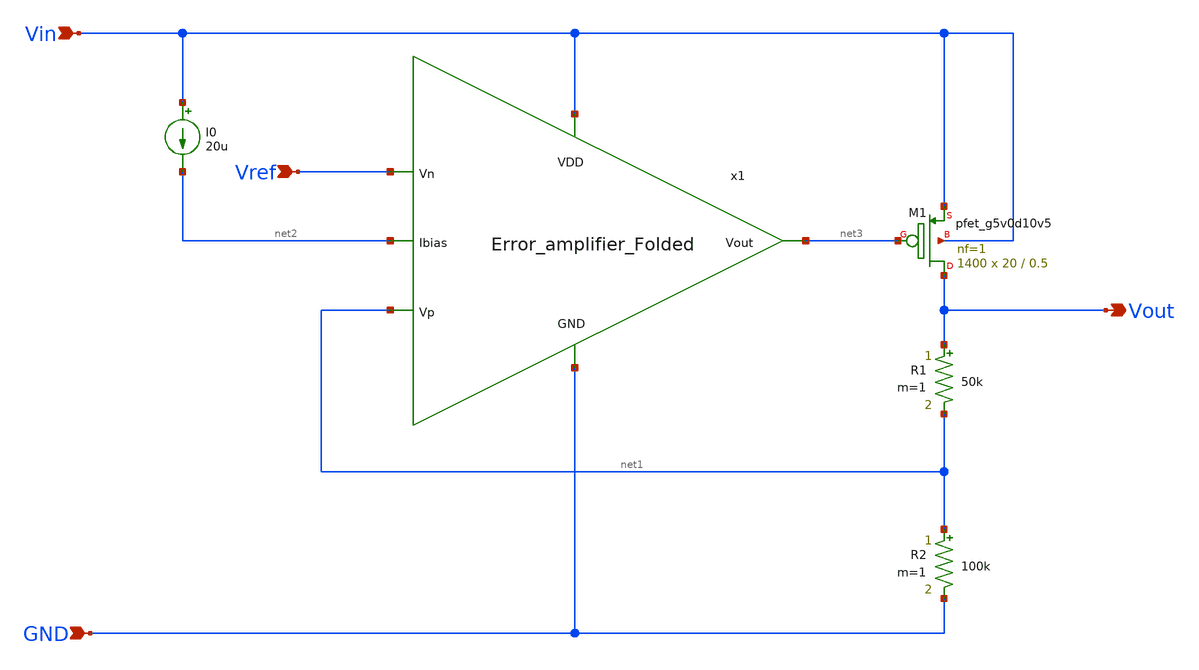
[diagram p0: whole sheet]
** sch_path: Analog_Blocks/LDO/Schematic/LDO_Miller_1.8v/LDO_test.sch
**.subckt LDO_test Vin GND Vout Vref
*.ipin Vin
*.ipin GND
*.opin Vout
*.ipin Vref
XM1 Vout net3 Vin Vin sky130_fd_pr__pfet_g5v0d10v5 L=0.5 W=20 nf=1 ad='int((nf+1)/2) * W/nf * 0.29' as='int((nf+2)/2) * W/nf * 0.29'
+ pd='2*int((nf+1)/2) * (W/nf + 0.29)' ps='2*int((nf+2)/2) * (W/nf + 0.29)' nrd='0.29 / W' nrs='0.29 / W'
+ sa=0 sb=0 sd=0 mult=1400 m=1400
R1 Vout net1 50k m=1
R2 net1 GND 100k m=1
I0 Vin net2 20u
x1 Vin net3 net1 Vref net2 GND Error_amplifier_Folded
**.ends

* expanding   symbol:
*+  /home/eslam/mabrains/Analog_blocks/Analog_Blocks/LDO/Schematic/LDO_Folded_1.8v/Error_amplifier_Folded.sym # of pins=6
** sym_path: Analog_Blocks/LDO/Schematic/LDO_Folded_1.8v/Error_amplifier_Folded.sym
** sch_path: Analog_Blocks/LDO/Schematic/LDO_Folded_1.8v/Error_amplifier_Folded.sch
.subckt Error_amplifier_Folded VDD Vout Vp Vn Ibias GND
*.ipin VDD
*.ipin GND
*.ipin Vp
*.ipin Vn
*.opin Vout
*.ipin Ibias
XM1 net3 Vp net1 GND sky130_fd_pr__nfet_g5v0d10v5 L=0.5 W=50 nf=1 ad='int((nf+1)/2) * W/nf * 0.29' as='int((nf+2)/2) * W/nf * 0.29'
+ pd='2*int((nf+1)/2) * (W/nf + 0.29)' ps='2*int((nf+2)/2) * (W/nf + 0.29)' nrd='0.29 / W' nrs='0.29 / W'
+ sa=0 sb=0 sd=0 mult=1 m=1
XM2 net2 Vn net1 GND sky130_fd_pr__nfet_g5v0d10v5 L=0.5 W=50 nf=1 ad='int((nf+1)/2) * W/nf * 0.29' as='int((nf+2)/2) * W/nf * 0.29'
+ pd='2*int((nf+1)/2) * (W/nf + 0.29)' ps='2*int((nf+2)/2) * (W/nf + 0.29)' nrd='0.29 / W' nrs='0.29 / W'
+ sa=0 sb=0 sd=0 mult=1 m=1
XM9 Vout net4 GND GND sky130_fd_pr__nfet_g5v0d10v5 L=2 W=6 nf=1 ad='int((nf+1)/2) * W/nf * 0.29' as='int((nf+2)/2) * W/nf * 0.29'
+ pd='2*int((nf+1)/2) * (W/nf + 0.29)' ps='2*int((nf+2)/2) * (W/nf + 0.29)' nrd='0.29 / W' nrs='0.29 / W'
+ sa=0 sb=0 sd=0 mult=1 m=1
XM6 net4 net6 net3 VDD sky130_fd_pr__pfet_g5v0d10v5 L=0.5 W=40 nf=1 ad='int((nf+1)/2) * W/nf * 0.29'
+ as='int((nf+2)/2) * W/nf * 0.29' pd='2*int((nf+1)/2) * (W/nf + 0.29)' ps='2*int((nf+2)/2) * (W/nf + 0.29)'
+ nrd='0.29 / W' nrs='0.29 / W' sa=0 sb=0 sd=0 mult=1 m=1
XM5 net2 net5 VDD VDD sky130_fd_pr__pfet_g5v0d10v5 L=0.5 W=40 nf=1 ad='int((nf+1)/2) * W/nf * 0.29' as='int((nf+2)/2) * W/nf * 0.29'
+ pd='2*int((nf+1)/2) * (W/nf + 0.29)' ps='2*int((nf+2)/2) * (W/nf + 0.29)' nrd='0.29 / W' nrs='0.29 / W'
+ sa=0 sb=0 sd=0 mult=1 m=1
XM4 net3 net5 VDD VDD sky130_fd_pr__pfet_g5v0d10v5 L=0.5 W=40 nf=1 ad='int((nf+1)/2) * W/nf * 0.29' as='int((nf+2)/2) * W/nf * 0.29'
+ pd='2*int((nf+1)/2) * (W/nf + 0.29)' ps='2*int((nf+2)/2) * (W/nf + 0.29)' nrd='0.29 / W' nrs='0.29 / W'
+ sa=0 sb=0 sd=0 mult=1 m=1
XM3 net1 Ibias GND GND sky130_fd_pr__nfet_g5v0d10v5 L=0.9 W=12 nf=1 ad='int((nf+1)/2) * W/nf * 0.29'
+ as='int((nf+2)/2) * W/nf * 0.29' pd='2*int((nf+1)/2) * (W/nf + 0.29)' ps='2*int((nf+2)/2) * (W/nf + 0.29)'
+ nrd='0.29 / W' nrs='0.29 / W' sa=0 sb=0 sd=0 mult=1 m=1
XM7 Vout net6 net2 VDD sky130_fd_pr__pfet_g5v0d10v5 L=0.5 W=40 nf=1 ad='int((nf+1)/2) * W/nf * 0.29'
+ as='int((nf+2)/2) * W/nf * 0.29' pd='2*int((nf+1)/2) * (W/nf + 0.29)' ps='2*int((nf+2)/2) * (W/nf + 0.29)'
+ nrd='0.29 / W' nrs='0.29 / W' sa=0 sb=0 sd=0 mult=1 m=1
XM8 net4 net4 GND GND sky130_fd_pr__nfet_g5v0d10v5 L=2 W=6 nf=1 ad='int((nf+1)/2) * W/nf * 0.29' as='int((nf+2)/2) * W/nf * 0.29'
+ pd='2*int((nf+1)/2) * (W/nf + 0.29)' ps='2*int((nf+2)/2) * (W/nf + 0.29)' nrd='0.29 / W' nrs='0.29 / W'
+ sa=0 sb=0 sd=0 mult=1 m=1
XM10 Ibias Ibias GND GND sky130_fd_pr__nfet_g5v0d10v5 L=0.9 W=12 nf=1 ad='int((nf+1)/2) * W/nf * 0.29'
+ as='int((nf+2)/2) * W/nf * 0.29' pd='2*int((nf+1)/2) * (W/nf + 0.29)' ps='2*int((nf+2)/2) * (W/nf + 0.29)'
+ nrd='0.29 / W' nrs='0.29 / W' sa=0 sb=0 sd=0 mult=1 m=1
XM11 net5 Ibias GND GND sky130_fd_pr__nfet_g5v0d10v5 L=0.9 W=6 nf=1 ad='int((nf+1)/2) * W/nf * 0.29'
+ as='int((nf+2)/2) * W/nf * 0.29' pd='2*int((nf+1)/2) * (W/nf + 0.29)' ps='2*int((nf+2)/2) * (W/nf + 0.29)'
+ nrd='0.29 / W' nrs='0.29 / W' sa=0 sb=0 sd=0 mult=1 m=1
XM12 net6 Ibias GND GND sky130_fd_pr__nfet_g5v0d10v5 L=0.9 W=6 nf=1 ad='int((nf+1)/2) * W/nf * 0.29'
+ as='int((nf+2)/2) * W/nf * 0.29' pd='2*int((nf+1)/2) * (W/nf + 0.29)' ps='2*int((nf+2)/2) * (W/nf + 0.29)'
+ nrd='0.29 / W' nrs='0.29 / W' sa=0 sb=0 sd=0 mult=1 m=1
XM13 net5 net5 VDD VDD sky130_fd_pr__pfet_g5v0d10v5 L=0.5 W=13.5 nf=1 ad='int((nf+1)/2) * W/nf * 0.29'
+ as='int((nf+2)/2) * W/nf * 0.29' pd='2*int((nf+1)/2) * (W/nf + 0.29)' ps='2*int((nf+2)/2) * (W/nf + 0.29)'
+ nrd='0.29 / W' nrs='0.29 / W' sa=0 sb=0 sd=0 mult=1 m=1
XM14 net6 net6 VDD VDD sky130_fd_pr__pfet_g5v0d10v5 L=1 W=2 nf=1 ad='int((nf+1)/2) * W/nf * 0.29' as='int((nf+2)/2) * W/nf * 0.29'
+ pd='2*int((nf+1)/2) * (W/nf + 0.29)' ps='2*int((nf+2)/2) * (W/nf + 0.29)' nrd='0.29 / W' nrs='0.29 / W'
+ sa=0 sb=0 sd=0 mult=1 m=1
.ends

.end
